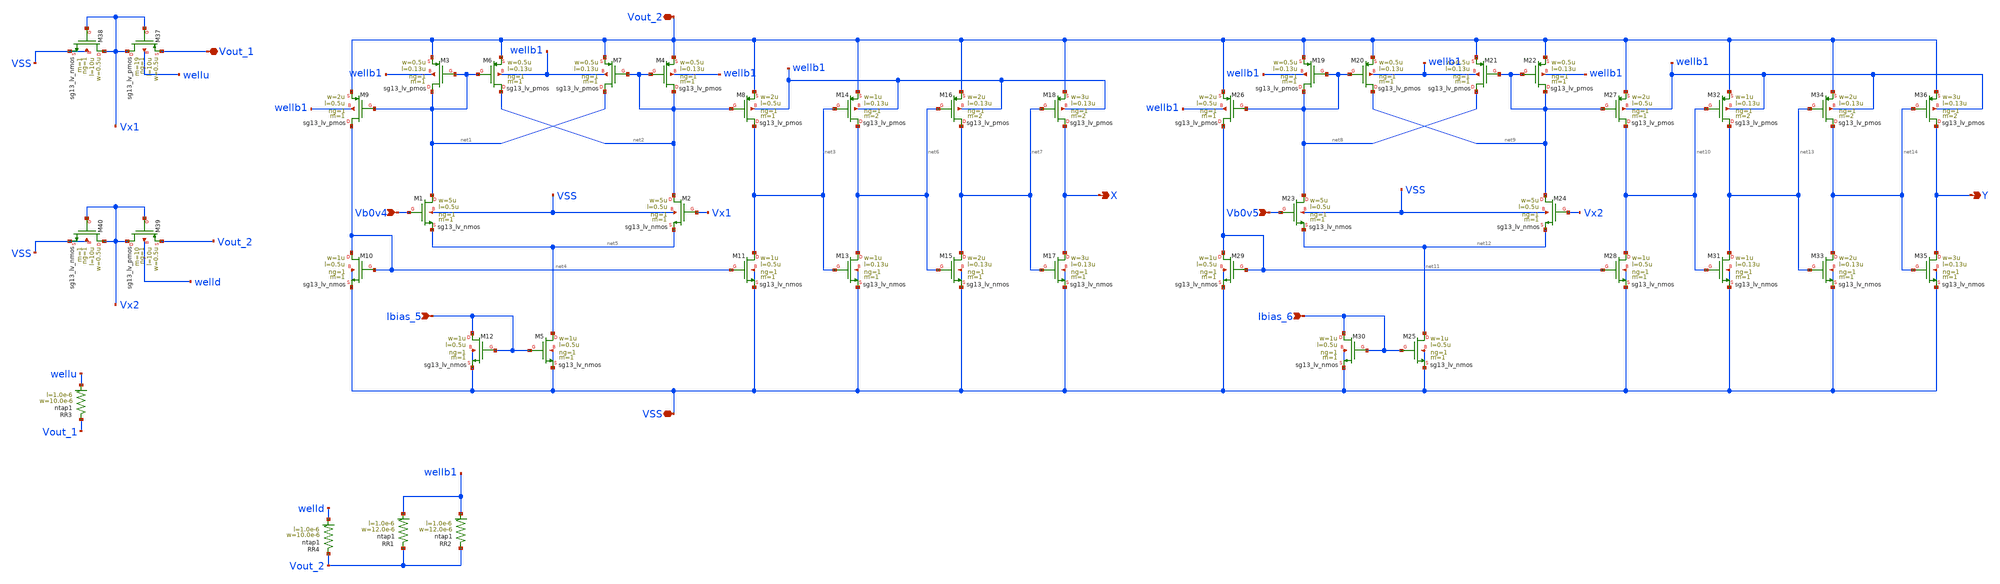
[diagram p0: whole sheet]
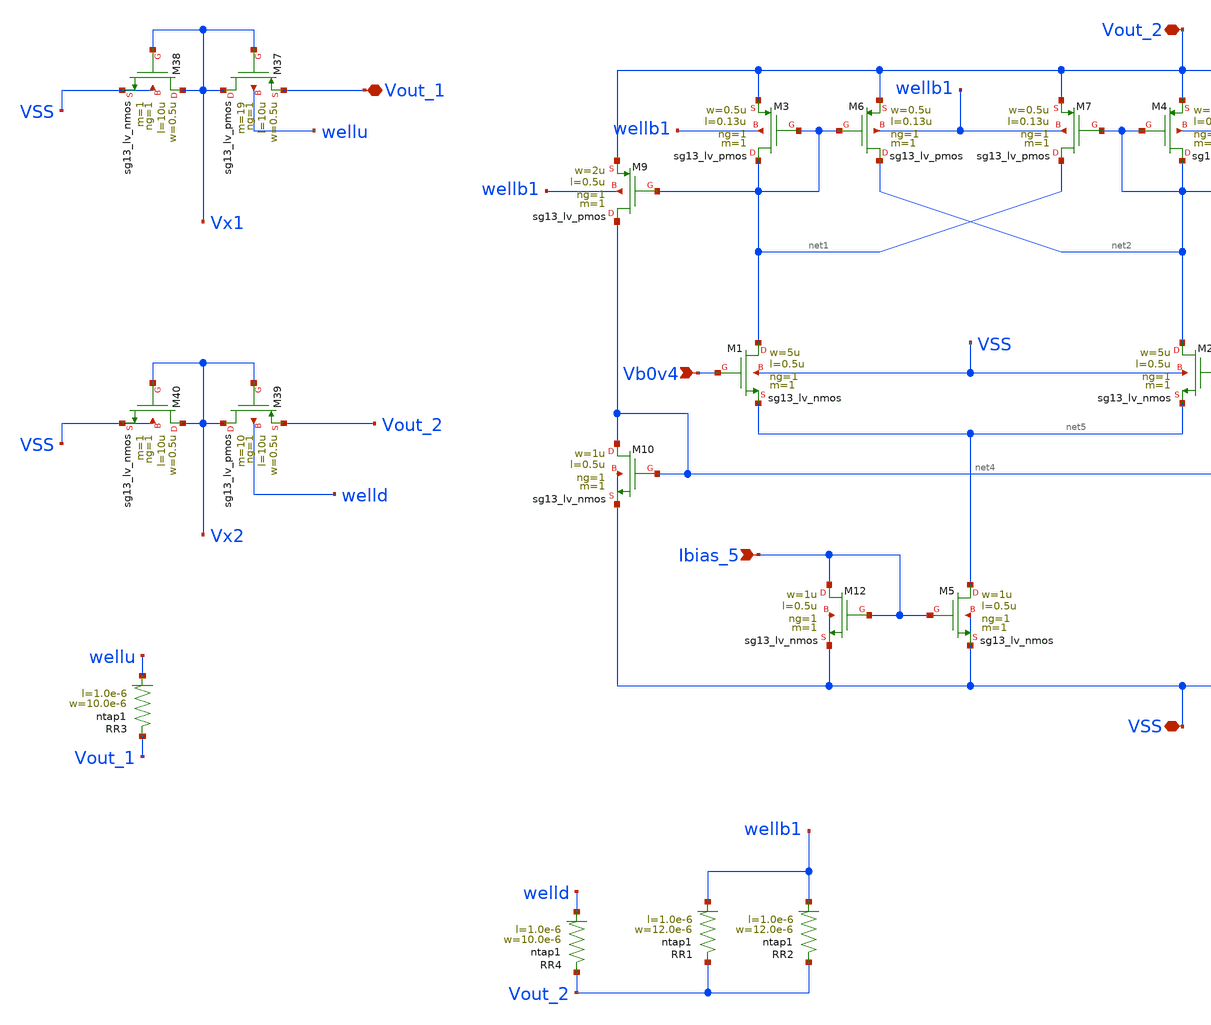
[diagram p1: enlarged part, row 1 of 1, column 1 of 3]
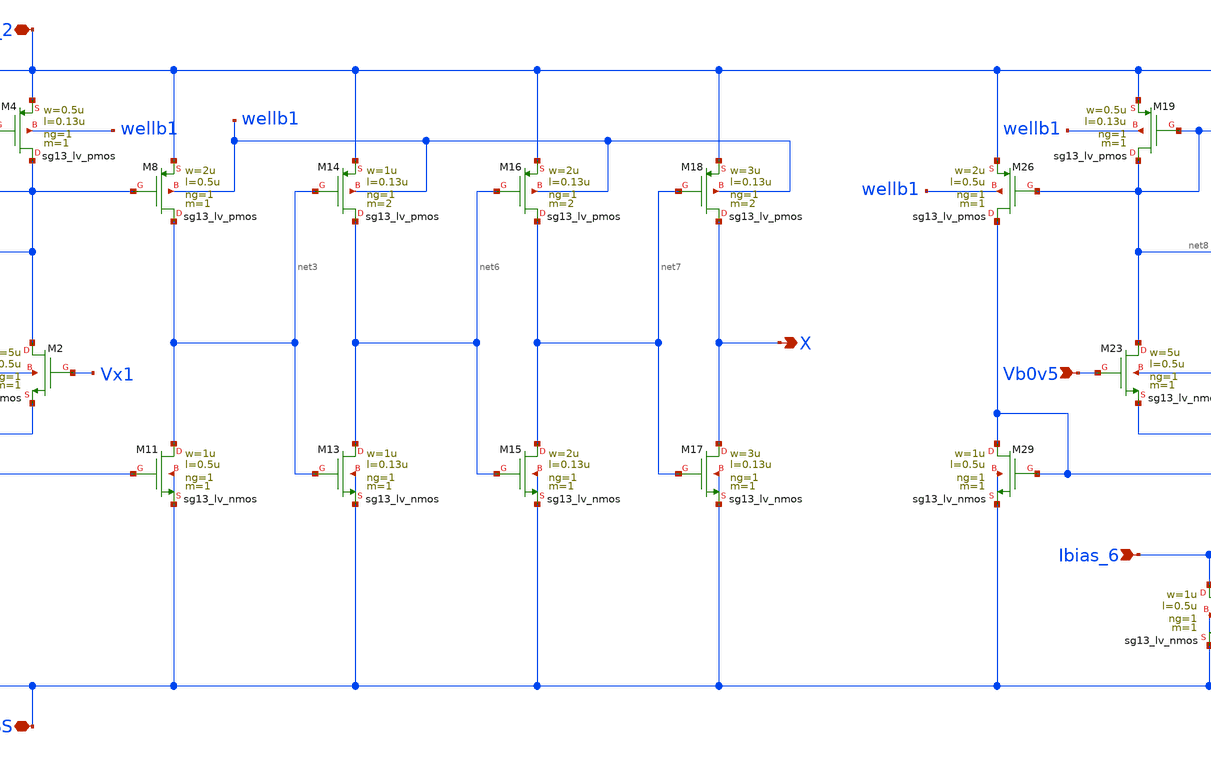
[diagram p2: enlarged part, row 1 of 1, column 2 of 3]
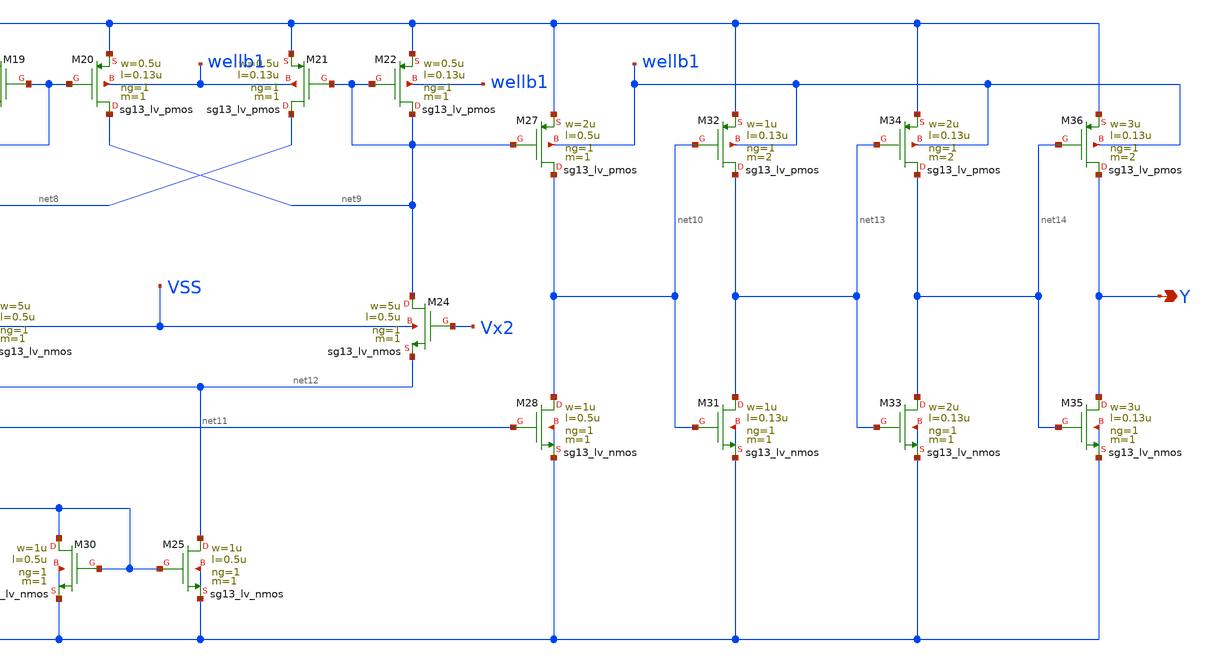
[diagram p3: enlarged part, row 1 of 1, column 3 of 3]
** sch_path: Layouts/Dig_control/dig_control_block1.sch
**.subckt dig_control_block1 Vb0v4 VSS Vout_2 X Y Vb0v5 Vout_1 Ibias_5 Ibias_6
*.ipin Vb0v4
*.iopin VSS
*.iopin Vout_2
*.opin X
*.opin Y
*.ipin Vb0v5
*.iopin Vout_1
*.ipin Ibias_5
*.ipin Ibias_6
XM3 net1 net1 Vout_2 wellb1 sg13_lv_pmos w=0.5u l=0.13u ng=1 m=1 mm_ok=1
XM6 net2 net1 Vout_2 wellb1 sg13_lv_pmos w=0.5u l=0.13u ng=1 m=1 mm_ok=1
XM7 net1 net2 Vout_2 wellb1 sg13_lv_pmos w=0.5u l=0.13u ng=1 m=1 mm_ok=1
XM4 net2 net2 Vout_2 wellb1 sg13_lv_pmos w=0.5u l=0.13u ng=1 m=1 mm_ok=1
XM1 net1 Vb0v4 net5 VSS sg13_lv_nmos w=5u l=0.5u ng=1 m=1 mm_ok=1
XM2 net2 Vx1 net5 VSS sg13_lv_nmos w=5u l=0.5u ng=1 m=1 mm_ok=1
XM5 net5 Ibias_5 VSS VSS sg13_lv_nmos w=1u l=0.5u ng=1 m=1 mm_ok=1
XM9 net4 net1 Vout_2 wellb1 sg13_lv_pmos w=2u l=0.5u ng=1 m=1 mm_ok=1
XM8 net3 net2 Vout_2 wellb1 sg13_lv_pmos w=2u l=0.5u ng=1 m=1 mm_ok=1
XM11 net3 net4 VSS VSS sg13_lv_nmos w=1u l=0.5u ng=1 m=1 mm_ok=1
XM10 net4 net4 VSS VSS sg13_lv_nmos w=1u l=0.5u ng=1 m=1 mm_ok=1
XM12 Ibias_5 Ibias_5 VSS VSS sg13_lv_nmos w=1u l=0.5u ng=1 m=1 mm_ok=1
XM13 net6 net3 VSS VSS sg13_lv_nmos w=1u l=0.13u ng=1 m=1 mm_ok=1
XM14 net6 net3 Vout_2 wellb1 sg13_lv_pmos w=1u l=0.13u ng=1 m=2 mm_ok=1
XM15 net7 net6 VSS VSS sg13_lv_nmos w=2u l=0.13u ng=1 m=1 mm_ok=1
XM16 net7 net6 Vout_2 wellb1 sg13_lv_pmos w=2u l=0.13u ng=1 m=2 mm_ok=1
XM17 X net7 VSS VSS sg13_lv_nmos w=3u l=0.13u ng=1 m=1 mm_ok=1
XM18 X net7 Vout_2 wellb1 sg13_lv_pmos w=3u l=0.13u ng=1 m=2 mm_ok=1
XM19 net8 net8 Vout_2 wellb1 sg13_lv_pmos w=0.5u l=0.13u ng=1 m=1 mm_ok=1
XM20 net9 net8 Vout_2 wellb1 sg13_lv_pmos w=0.5u l=0.13u ng=1 m=1 mm_ok=1
XM21 net8 net9 Vout_2 wellb1 sg13_lv_pmos w=0.5u l=0.13u ng=1 m=1 mm_ok=1
XM22 net9 net9 Vout_2 wellb1 sg13_lv_pmos w=0.5u l=0.13u ng=1 m=1 mm_ok=1
XM23 net8 Vb0v5 net12 VSS sg13_lv_nmos w=5u l=0.5u ng=1 m=1 mm_ok=1
XM24 net9 Vx2 net12 VSS sg13_lv_nmos w=5u l=0.5u ng=1 m=1 mm_ok=1
XM25 net12 Ibias_6 VSS VSS sg13_lv_nmos w=1u l=0.5u ng=1 m=1 mm_ok=1
XM26 net11 net8 Vout_2 wellb1 sg13_lv_pmos w=2u l=0.5u ng=1 m=1 mm_ok=1
XM27 net10 net9 Vout_2 wellb1 sg13_lv_pmos w=2u l=0.5u ng=1 m=1 mm_ok=1
XM28 net10 net11 VSS VSS sg13_lv_nmos w=1u l=0.5u ng=1 m=1 mm_ok=1
XM29 net11 net11 VSS VSS sg13_lv_nmos w=1u l=0.5u ng=1 m=1 mm_ok=1
XM30 Ibias_6 Ibias_6 VSS VSS sg13_lv_nmos w=1u l=0.5u ng=1 m=1 mm_ok=1
XM31 net13 net10 VSS VSS sg13_lv_nmos w=1u l=0.13u ng=1 m=1 mm_ok=1
XM32 net13 net10 Vout_2 wellb1 sg13_lv_pmos w=1u l=0.13u ng=1 m=2 mm_ok=1
XM33 net14 net13 VSS VSS sg13_lv_nmos w=2u l=0.13u ng=1 m=1 mm_ok=1
XM34 net14 net13 Vout_2 wellb1 sg13_lv_pmos w=2u l=0.13u ng=1 m=2 mm_ok=1
XM35 Y net14 VSS VSS sg13_lv_nmos w=3u l=0.13u ng=1 m=1 mm_ok=1
XM36 Y net14 Vout_2 wellb1 sg13_lv_pmos w=3u l=0.13u ng=1 m=2 mm_ok=1
XM37 Vx1 Vx1 Vout_1 wellu sg13_lv_pmos w=0.5u l=10u ng=1 m=19 mm_ok=1
XM38 Vx1 Vx1 VSS VSS sg13_lv_nmos w=0.5u l=10u ng=1 m=1 mm_ok=1
XM39 Vx2 Vx2 Vout_2 welld sg13_lv_pmos w=0.5u l=10u ng=1 m=10 mm_ok=1
XM40 Vx2 Vx2 VSS VSS sg13_lv_nmos w=0.5u l=10u ng=1 m=1 mm_ok=1
XR1 Vout_2 wellb1 ntap1 R=25.79 w=12.0e-6 l=1.0e-6
XR2 Vout_2 wellb1 ntap1 R=25.79 w=12.0e-6 l=1.0e-6
XR3 Vout_1 wellu ntap1 R=30.62 w=10.0e-6 l=1.0e-6
XR4 Vout_2 welld ntap1 R=30.62 w=10.0e-6 l=1.0e-6
**.ends
.end
